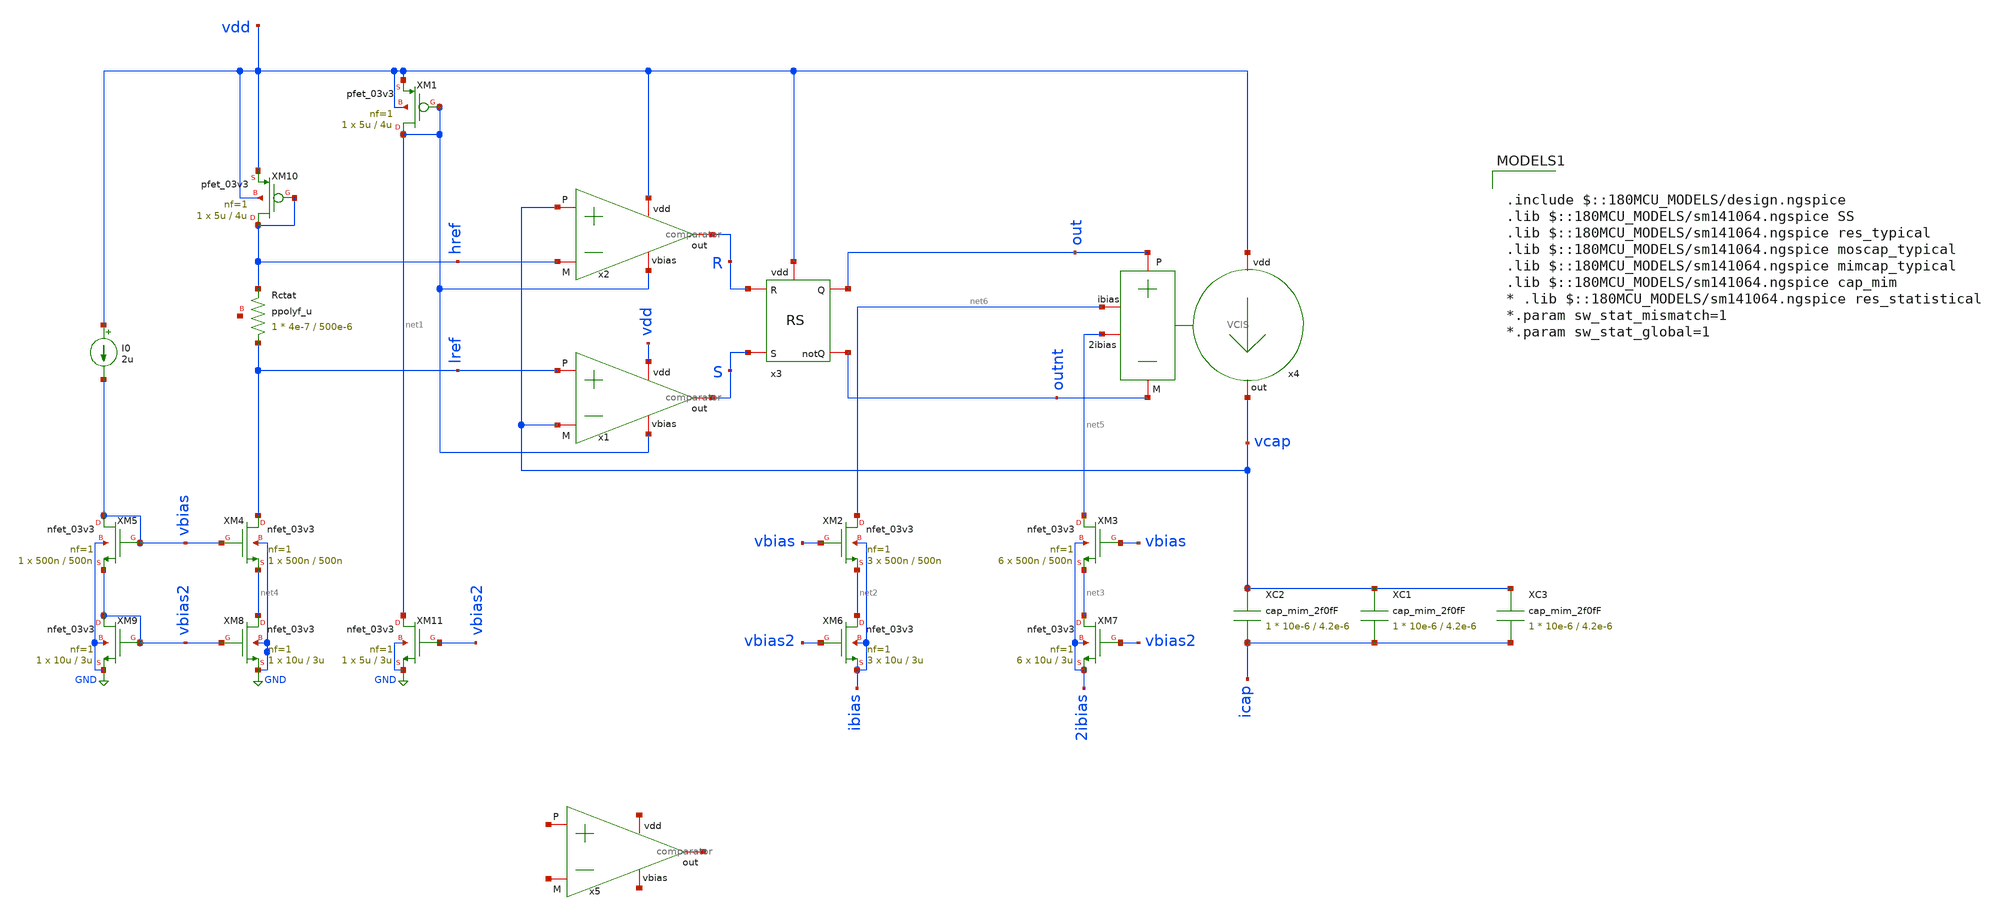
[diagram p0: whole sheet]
** sch_path: Clock_Reference/xschem/clockGenerator.sch
**.subckt clockGenerator
XM1 net1 net1 vdd vdd pfet_03v3 L=4u W=5u nf=1 ad='int((nf+1)/2) * W/nf * 0.18u' as='int((nf+2)/2) * W/nf * 0.18u'
+ pd='2*int((nf+1)/2) * (W/nf + 0.18u)' ps='2*int((nf+2)/2) * (W/nf + 0.18u)' nrd='0.18u / W' nrs='0.18u / W'
+ sa=0 sb=0 sd=0 m=1
XM2 net6 vbias net2 ibias nfet_03v3 L=500n W=500n nf=1 ad='int((nf+1)/2) * W/nf * 0.18u' as='int((nf+2)/2) * W/nf * 0.18u'
+ pd='2*int((nf+1)/2) * (W/nf + 0.18u)' ps='2*int((nf+2)/2) * (W/nf + 0.18u)' nrd='0.18u / W' nrs='0.18u / W'
+ sa=0 sb=0 sd=0 m=3
XM3 net5 vbias net3 2ibias nfet_03v3 L=500n W=500n nf=1 ad='int((nf+1)/2) * W/nf * 0.18u' as='int((nf+2)/2) * W/nf * 0.18u'
+ pd='2*int((nf+1)/2) * (W/nf + 0.18u)' ps='2*int((nf+2)/2) * (W/nf + 0.18u)' nrd='0.18u / W' nrs='0.18u / W'
+ sa=0 sb=0 sd=0 m=6
XM4 lref vbias net4 GND nfet_03v3 L=500n W=500n nf=1 ad='int((nf+1)/2) * W/nf * 0.18u' as='int((nf+2)/2) * W/nf * 0.18u'
+ pd='2*int((nf+1)/2) * (W/nf + 0.18u)' ps='2*int((nf+2)/2) * (W/nf + 0.18u)' nrd='0.18u / W' nrs='0.18u / W'
+ sa=0 sb=0 sd=0 m=1
XM5 vbias vbias vbias2 GND nfet_03v3 L=500n W=500n nf=1 ad='int((nf+1)/2) * W/nf * 0.18u' as='int((nf+2)/2) * W/nf * 0.18u'
+ pd='2*int((nf+1)/2) * (W/nf + 0.18u)' ps='2*int((nf+2)/2) * (W/nf + 0.18u)' nrd='0.18u / W' nrs='0.18u / W'
+ sa=0 sb=0 sd=0 m=1
I0 vdd vbias 2u
XM6 net2 vbias2 ibias ibias nfet_03v3 L=3u W=10u nf=1 ad='int((nf+1)/2) * W/nf * 0.18u' as='int((nf+2)/2) * W/nf * 0.18u'
+ pd='2*int((nf+1)/2) * (W/nf + 0.18u)' ps='2*int((nf+2)/2) * (W/nf + 0.18u)' nrd='0.18u / W' nrs='0.18u / W'
+ sa=0 sb=0 sd=0 m=3
XM7 net3 vbias2 2ibias 2ibias nfet_03v3 L=3u W=10u nf=1 ad='int((nf+1)/2) * W/nf * 0.18u' as='int((nf+2)/2) * W/nf * 0.18u'
+ pd='2*int((nf+1)/2) * (W/nf + 0.18u)' ps='2*int((nf+2)/2) * (W/nf + 0.18u)' nrd='0.18u / W' nrs='0.18u / W'
+ sa=0 sb=0 sd=0 m=6
XM8 net4 vbias2 GND GND nfet_03v3 L=3u W=10u nf=1 ad='int((nf+1)/2) * W/nf * 0.18u' as='int((nf+2)/2) * W/nf * 0.18u'
+ pd='2*int((nf+1)/2) * (W/nf + 0.18u)' ps='2*int((nf+2)/2) * (W/nf + 0.18u)' nrd='0.18u / W' nrs='0.18u / W'
+ sa=0 sb=0 sd=0 m=1
XM9 vbias2 vbias2 GND GND nfet_03v3 L=3u W=10u nf=1 ad='int((nf+1)/2) * W/nf * 0.18u' as='int((nf+2)/2) * W/nf * 0.18u'
+ pd='2*int((nf+1)/2) * (W/nf + 0.18u)' ps='2*int((nf+2)/2) * (W/nf + 0.18u)' nrd='0.18u / W' nrs='0.18u / W'
+ sa=0 sb=0 sd=0 m=1
XRctat lref href net7 ppolyf_u r_width=4e-7 r_length=500e-6 m=1
XM10 href href vdd vdd pfet_03v3 L=4u W=5u nf=1 ad='int((nf+1)/2) * W/nf * 0.18u' as='int((nf+2)/2) * W/nf * 0.18u'
+ pd='2*int((nf+1)/2) * (W/nf + 0.18u)' ps='2*int((nf+2)/2) * (W/nf + 0.18u)' nrd='0.18u / W' nrs='0.18u / W'
+ sa=0 sb=0 sd=0 m=1
XM11 net1 vbias2 GND GND nfet_03v3 L=3u W=5u nf=1 ad='int((nf+1)/2) * W/nf * 0.18u' as='int((nf+2)/2) * W/nf * 0.18u'
+ pd='2*int((nf+1)/2) * (W/nf + 0.18u)' ps='2*int((nf+2)/2) * (W/nf + 0.18u)' nrd='0.18u / W' nrs='0.18u / W'
+ sa=0 sb=0 sd=0 m=1
XC2 vcap icap cap_mim_2f0fF c_width=10e-6 c_length=4.2e-6 m=1
XC1 vcap icap cap_mim_2f0fF c_width=10e-6 c_length=4.2e-6 m=1
XC3 vcap icap cap_mim_2f0fF c_width=10e-6 c_length=4.2e-6 m=1
x4 vdd vcap out outnt net6 net5 VCIS
x3 vdd R S out outnt RS
x1 vdd net1 lref vcap S comparator
x2 vdd net1 vcap href R comparator
x5 net8 net9 net10 net11 net12 comparator
**** begin user architecture code


vvdd vdd 0 3.3
vcurr curr 0 0
vibias ibias 0 0
v2ibias 2ibias 0 0
vicap icap 0 0

.control
let temperature = -40

while temperature<130
set temp = $&temperature
tran 5p 500n
set filetype = binary
write transient[$&temperature].raw
wrdata /home/cesaralbuquerque/Desktop/out/transient[$&temperature].txt V(out)
let temperature = temperature + 20
end


.endc
.save all



.include $::180MCU_MODELS/design.ngspice
.lib $::180MCU_MODELS/sm141064.ngspice SS
.lib $::180MCU_MODELS/sm141064.ngspice res_typical
.lib $::180MCU_MODELS/sm141064.ngspice moscap_typical
.lib $::180MCU_MODELS/sm141064.ngspice mimcap_typical
.lib $::180MCU_MODELS/sm141064.ngspice cap_mim
* .lib $::180MCU_MODELS/sm141064.ngspice res_statistical
*.param sw_stat_mismatch=1
*.param sw_stat_global=1

**** end user architecture code
**.ends
.GLOBAL GND
.end
